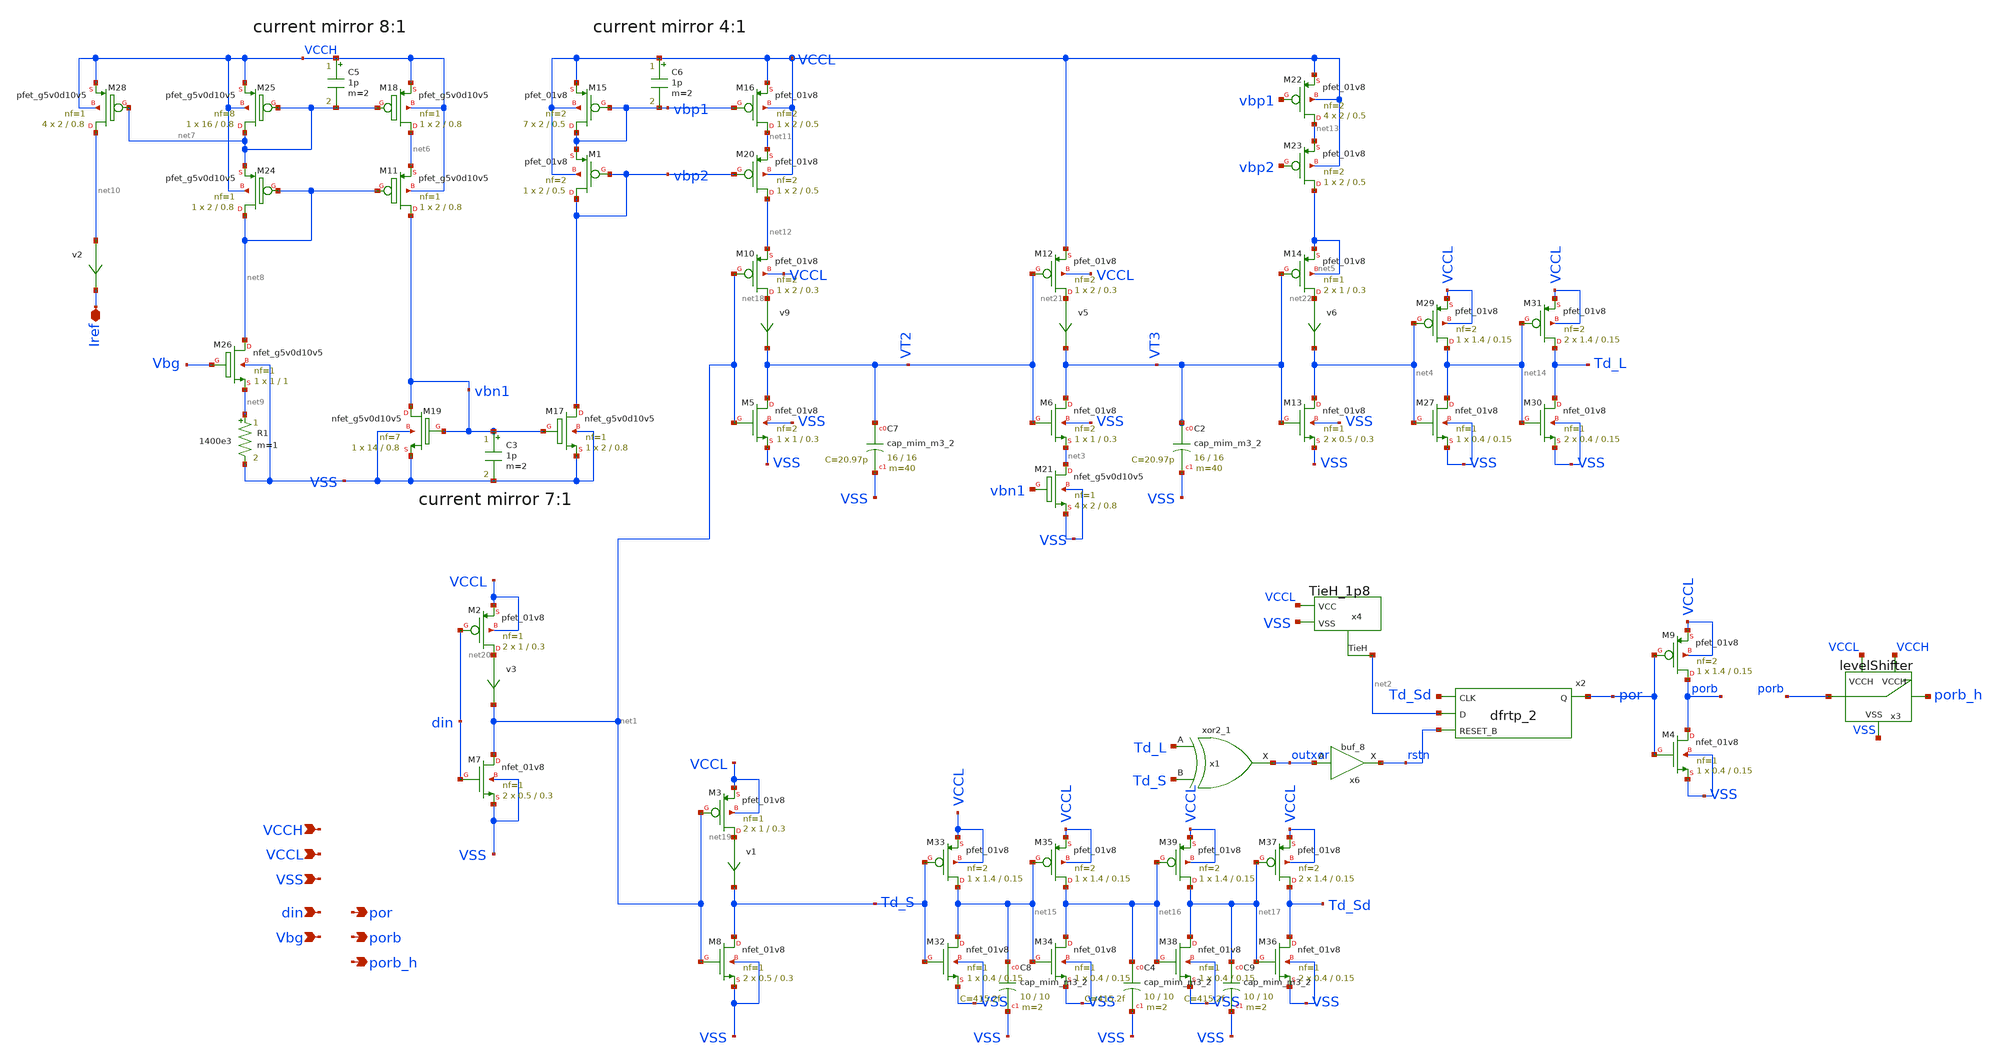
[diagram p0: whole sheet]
** sch_path: xschem/delayPulse.sch
**.subckt delayPulse VCCL VSS din Vbg por VCCH porb porb_h Iref
*.ipin VCCL
*.ipin VSS
*.ipin din
*.ipin Vbg
*.opin por
*.ipin VCCH
*.opin porb
*.opin porb_h
*.iopin Iref
v9 net18 VT2 0
.save i(v9)
v1 net19 Td_S 0
.save i(v1)
x2 Td_Sd net2 rstn VSS VSS VCCL VCCL por sky130_fd_sc_hd__dfrtp_2
v3 net20 net1 0
.save i(v3)
x1 Td_L Td_S VSS VSS VCCL VCCL outxor sky130_fd_sc_hd__xor2_1
x3 porb porb_h VCCL VSS VCCH levelShifter
XM2 net20 din VCCL VCCL sky130_fd_pr__pfet_01v8 L=0.3 W=1 nf=1 ad='int((nf+1)/2) * W/nf * 0.29' as='int((nf+2)/2) * W/nf * 0.29'
+ pd='2*int((nf+1)/2) * (W/nf + 0.29)' ps='2*int((nf+2)/2) * (W/nf + 0.29)' nrd='0.29 / W' nrs='0.29 / W'
+ sa=0 sb=0 sd=0 mult=2 m=2
XM3 net19 net1 VCCL VCCL sky130_fd_pr__pfet_01v8 L=0.3 W=1 nf=1 ad='int((nf+1)/2) * W/nf * 0.29' as='int((nf+2)/2) * W/nf * 0.29'
+ pd='2*int((nf+1)/2) * (W/nf + 0.29)' ps='2*int((nf+2)/2) * (W/nf + 0.29)' nrd='0.29 / W' nrs='0.29 / W'
+ sa=0 sb=0 sd=0 mult=2 m=2
XM5 VT2 net1 VSS VSS sky130_fd_pr__nfet_01v8 L=0.3 W=1 nf=2 ad='int((nf+1)/2) * W/nf * 0.29' as='int((nf+2)/2) * W/nf * 0.29'
+ pd='2*int((nf+1)/2) * (W/nf + 0.29)' ps='2*int((nf+2)/2) * (W/nf + 0.29)' nrd='0.29 / W' nrs='0.29 / W'
+ sa=0 sb=0 sd=0 mult=1 m=1
XM7 net1 din VSS VSS sky130_fd_pr__nfet_01v8 L=0.3 W=0.5 nf=1 ad='int((nf+1)/2) * W/nf * 0.29' as='int((nf+2)/2) * W/nf * 0.29'
+ pd='2*int((nf+1)/2) * (W/nf + 0.29)' ps='2*int((nf+2)/2) * (W/nf + 0.29)' nrd='0.29 / W' nrs='0.29 / W'
+ sa=0 sb=0 sd=0 mult=2 m=2
XM8 Td_S net1 VSS VSS sky130_fd_pr__nfet_01v8 L=0.3 W=0.5 nf=1 ad='int((nf+1)/2) * W/nf * 0.29' as='int((nf+2)/2) * W/nf * 0.29'
+ pd='2*int((nf+1)/2) * (W/nf + 0.29)' ps='2*int((nf+2)/2) * (W/nf + 0.29)' nrd='0.29 / W' nrs='0.29 / W'
+ sa=0 sb=0 sd=0 mult=2 m=2
XM10 net18 net1 net12 VCCL sky130_fd_pr__pfet_01v8 L=0.3 W=2 nf=2 ad='int((nf+1)/2) * W/nf * 0.29' as='int((nf+2)/2) * W/nf * 0.29'
+ pd='2*int((nf+1)/2) * (W/nf + 0.29)' ps='2*int((nf+2)/2) * (W/nf + 0.29)' nrd='0.29 / W' nrs='0.29 / W'
+ sa=0 sb=0 sd=0 mult=1 m=1
v5 net21 VT3 0
.save i(v5)
v6 net22 net4 0
.save i(v6)
XM13 net4 VT3 VSS VSS sky130_fd_pr__nfet_01v8 L=0.3 W=0.5 nf=1 ad='int((nf+1)/2) * W/nf * 0.29' as='int((nf+2)/2) * W/nf * 0.29'
+ pd='2*int((nf+1)/2) * (W/nf + 0.29)' ps='2*int((nf+2)/2) * (W/nf + 0.29)' nrd='0.29 / W' nrs='0.29 / W'
+ sa=0 sb=0 sd=0 mult=2 m=2
XM14 net22 VT3 net5 net5 sky130_fd_pr__pfet_01v8 L=0.3 W=1 nf=1 ad='int((nf+1)/2) * W/nf * 0.29' as='int((nf+2)/2) * W/nf * 0.29'
+ pd='2*int((nf+1)/2) * (W/nf + 0.29)' ps='2*int((nf+2)/2) * (W/nf + 0.29)' nrd='0.29 / W' nrs='0.29 / W'
+ sa=0 sb=0 sd=0 mult=2 m=2
x4 net2 VSS VCCL TieH_1p8
XM4 porb por VSS VSS sky130_fd_pr__nfet_01v8 L=0.15 W=0.4 nf=1 ad='int((nf+1)/2) * W/nf * 0.29' as='int((nf+2)/2) * W/nf * 0.29'
+ pd='2*int((nf+1)/2) * (W/nf + 0.29)' ps='2*int((nf+2)/2) * (W/nf + 0.29)' nrd='0.29 / W' nrs='0.29 / W'
+ sa=0 sb=0 sd=0 mult=1 m=1
XM9 porb por VCCL VCCL sky130_fd_pr__pfet_01v8 L=0.15 W=1.4 nf=2 ad='int((nf+1)/2) * W/nf * 0.29' as='int((nf+2)/2) * W/nf * 0.29'
+ pd='2*int((nf+1)/2) * (W/nf + 0.29)' ps='2*int((nf+2)/2) * (W/nf + 0.29)' nrd='0.29 / W' nrs='0.29 / W'
+ sa=0 sb=0 sd=0 mult=1 m=1
v2 net10 Iref 0
.save i(v2)
XM11 vbn1 net8 net6 VCCH sky130_fd_pr__pfet_g5v0d10v5 L=0.8 W=2 nf=1 ad='int((nf+1)/2) * W/nf * 0.29'
+ as='int((nf+2)/2) * W/nf * 0.29' pd='2*int((nf+1)/2) * (W/nf + 0.29)' ps='2*int((nf+2)/2) * (W/nf + 0.29)'
+ nrd='0.29 / W' nrs='0.29 / W' sa=0 sb=0 sd=0 mult=1 m=1
XM17 vbp2 vbn1 VSS VSS sky130_fd_pr__nfet_g5v0d10v5 L=0.8 W=2 nf=1 ad='int((nf+1)/2) * W/nf * 0.29' as='int((nf+2)/2) * W/nf * 0.29'
+ pd='2*int((nf+1)/2) * (W/nf + 0.29)' ps='2*int((nf+2)/2) * (W/nf + 0.29)' nrd='0.29 / W' nrs='0.29 / W'
+ sa=0 sb=0 sd=0 mult=1 m=1
XM18 net6 net7 VCCH VCCH sky130_fd_pr__pfet_g5v0d10v5 L=0.8 W=2 nf=1 ad='int((nf+1)/2) * W/nf * 0.29'
+ as='int((nf+2)/2) * W/nf * 0.29' pd='2*int((nf+1)/2) * (W/nf + 0.29)' ps='2*int((nf+2)/2) * (W/nf + 0.29)'
+ nrd='0.29 / W' nrs='0.29 / W' sa=0 sb=0 sd=0 mult=1 m=1
XM19 vbn1 vbn1 VSS VSS sky130_fd_pr__nfet_g5v0d10v5 L=0.8 W=14 nf=7 ad='int((nf+1)/2) * W/nf * 0.29'
+ as='int((nf+2)/2) * W/nf * 0.29' pd='2*int((nf+1)/2) * (W/nf + 0.29)' ps='2*int((nf+2)/2) * (W/nf + 0.29)'
+ nrd='0.29 / W' nrs='0.29 / W' sa=0 sb=0 sd=0 mult=1 m=1
XM24 net8 net8 net7 VCCH sky130_fd_pr__pfet_g5v0d10v5 L=0.8 W=2 nf=1 ad='int((nf+1)/2) * W/nf * 0.29'
+ as='int((nf+2)/2) * W/nf * 0.29' pd='2*int((nf+1)/2) * (W/nf + 0.29)' ps='2*int((nf+2)/2) * (W/nf + 0.29)'
+ nrd='0.29 / W' nrs='0.29 / W' sa=0 sb=0 sd=0 mult=1 m=1
XM25 net7 net7 VCCH VCCH sky130_fd_pr__pfet_g5v0d10v5 L=0.8 W=16 nf=8 ad='int((nf+1)/2) * W/nf * 0.29'
+ as='int((nf+2)/2) * W/nf * 0.29' pd='2*int((nf+1)/2) * (W/nf + 0.29)' ps='2*int((nf+2)/2) * (W/nf + 0.29)'
+ nrd='0.29 / W' nrs='0.29 / W' sa=0 sb=0 sd=0 mult=1 m=1
XM26 net8 Vbg net9 VSS sky130_fd_pr__nfet_g5v0d10v5 L=1 W=1 nf=1 ad='int((nf+1)/2) * W/nf * 0.29' as='int((nf+2)/2) * W/nf * 0.29'
+ pd='2*int((nf+1)/2) * (W/nf + 0.29)' ps='2*int((nf+2)/2) * (W/nf + 0.29)' nrd='0.29 / W' nrs='0.29 / W'
+ sa=0 sb=0 sd=0 mult=1 m=1
R1 net9 VSS 1400e3 m=1
XM28 net10 net7 VCCH VCCH sky130_fd_pr__pfet_g5v0d10v5 L=0.8 W=2 nf=1 ad='int((nf+1)/2) * W/nf * 0.29'
+ as='int((nf+2)/2) * W/nf * 0.29' pd='2*int((nf+1)/2) * (W/nf + 0.29)' ps='2*int((nf+2)/2) * (W/nf + 0.29)'
+ nrd='0.29 / W' nrs='0.29 / W' sa=0 sb=0 sd=0 mult=4 m=4
XM6 VT3 VT2 net3 VSS sky130_fd_pr__nfet_01v8 L=0.3 W=1 nf=2 ad='int((nf+1)/2) * W/nf * 0.29' as='int((nf+2)/2) * W/nf * 0.29'
+ pd='2*int((nf+1)/2) * (W/nf + 0.29)' ps='2*int((nf+2)/2) * (W/nf + 0.29)' nrd='0.29 / W' nrs='0.29 / W'
+ sa=0 sb=0 sd=0 mult=1 m=1
XM12 net21 VT2 VCCL VCCL sky130_fd_pr__pfet_01v8 L=0.3 W=2 nf=2 ad='int((nf+1)/2) * W/nf * 0.29' as='int((nf+2)/2) * W/nf * 0.29'
+ pd='2*int((nf+1)/2) * (W/nf + 0.29)' ps='2*int((nf+2)/2) * (W/nf + 0.29)' nrd='0.29 / W' nrs='0.29 / W'
+ sa=0 sb=0 sd=0 mult=1 m=1
XM1 vbp2 vbp2 vbp1 VCCL sky130_fd_pr__pfet_01v8 L=0.5 W=2 nf=2 ad='int((nf+1)/2) * W/nf * 0.29' as='int((nf+2)/2) * W/nf * 0.29'
+ pd='2*int((nf+1)/2) * (W/nf + 0.29)' ps='2*int((nf+2)/2) * (W/nf + 0.29)' nrd='0.29 / W' nrs='0.29 / W'
+ sa=0 sb=0 sd=0 mult=1 m=1
XM15 vbp1 vbp1 VCCL VCCL sky130_fd_pr__pfet_01v8 L=0.5 W=2 nf=2 ad='int((nf+1)/2) * W/nf * 0.29' as='int((nf+2)/2) * W/nf * 0.29'
+ pd='2*int((nf+1)/2) * (W/nf + 0.29)' ps='2*int((nf+2)/2) * (W/nf + 0.29)' nrd='0.29 / W' nrs='0.29 / W'
+ sa=0 sb=0 sd=0 mult=7 m=7
XM16 net11 vbp1 VCCL VCCL sky130_fd_pr__pfet_01v8 L=0.5 W=2 nf=2 ad='int((nf+1)/2) * W/nf * 0.29' as='int((nf+2)/2) * W/nf * 0.29'
+ pd='2*int((nf+1)/2) * (W/nf + 0.29)' ps='2*int((nf+2)/2) * (W/nf + 0.29)' nrd='0.29 / W' nrs='0.29 / W'
+ sa=0 sb=0 sd=0 mult=1 m=1
XM20 net12 vbp2 net11 VCCL sky130_fd_pr__pfet_01v8 L=0.5 W=2 nf=2 ad='int((nf+1)/2) * W/nf * 0.29' as='int((nf+2)/2) * W/nf * 0.29'
+ pd='2*int((nf+1)/2) * (W/nf + 0.29)' ps='2*int((nf+2)/2) * (W/nf + 0.29)' nrd='0.29 / W' nrs='0.29 / W'
+ sa=0 sb=0 sd=0 mult=1 m=1
XM21 net3 vbn1 VSS VSS sky130_fd_pr__nfet_g5v0d10v5 L=0.8 W=2 nf=1 ad='int((nf+1)/2) * W/nf * 0.29' as='int((nf+2)/2) * W/nf * 0.29'
+ pd='2*int((nf+1)/2) * (W/nf + 0.29)' ps='2*int((nf+2)/2) * (W/nf + 0.29)' nrd='0.29 / W' nrs='0.29 / W'
+ sa=0 sb=0 sd=0 mult=4 m=4
C3 vbn1 VSS 1p m=2
C5 VCCH net7 1p m=2
C6 VCCL vbp1 1p m=2
XM22 net13 vbp1 VCCL VCCL sky130_fd_pr__pfet_01v8 L=0.5 W=2 nf=2 ad='int((nf+1)/2) * W/nf * 0.29' as='int((nf+2)/2) * W/nf * 0.29'
+ pd='2*int((nf+1)/2) * (W/nf + 0.29)' ps='2*int((nf+2)/2) * (W/nf + 0.29)' nrd='0.29 / W' nrs='0.29 / W'
+ sa=0 sb=0 sd=0 mult=4 m=4
XM23 net5 vbp2 net13 VCCL sky130_fd_pr__pfet_01v8 L=0.5 W=2 nf=2 ad='int((nf+1)/2) * W/nf * 0.29' as='int((nf+2)/2) * W/nf * 0.29'
+ pd='2*int((nf+1)/2) * (W/nf + 0.29)' ps='2*int((nf+2)/2) * (W/nf + 0.29)' nrd='0.29 / W' nrs='0.29 / W'
+ sa=0 sb=0 sd=0 mult=1 m=1
XM27 net14 net4 VSS VSS sky130_fd_pr__nfet_01v8 L=0.15 W=0.4 nf=1 ad='int((nf+1)/2) * W/nf * 0.29' as='int((nf+2)/2) * W/nf * 0.29'
+ pd='2*int((nf+1)/2) * (W/nf + 0.29)' ps='2*int((nf+2)/2) * (W/nf + 0.29)' nrd='0.29 / W' nrs='0.29 / W'
+ sa=0 sb=0 sd=0 mult=1 m=1
XM29 net14 net4 VCCL VCCL sky130_fd_pr__pfet_01v8 L=0.15 W=1.4 nf=2 ad='int((nf+1)/2) * W/nf * 0.29'
+ as='int((nf+2)/2) * W/nf * 0.29' pd='2*int((nf+1)/2) * (W/nf + 0.29)' ps='2*int((nf+2)/2) * (W/nf + 0.29)'
+ nrd='0.29 / W' nrs='0.29 / W' sa=0 sb=0 sd=0 mult=1 m=1
XM30 Td_L net14 VSS VSS sky130_fd_pr__nfet_01v8 L=0.15 W=0.4 nf=1 ad='int((nf+1)/2) * W/nf * 0.29' as='int((nf+2)/2) * W/nf * 0.29'
+ pd='2*int((nf+1)/2) * (W/nf + 0.29)' ps='2*int((nf+2)/2) * (W/nf + 0.29)' nrd='0.29 / W' nrs='0.29 / W'
+ sa=0 sb=0 sd=0 mult=2 m=2
XM31 Td_L net14 VCCL VCCL sky130_fd_pr__pfet_01v8 L=0.15 W=1.4 nf=2 ad='int((nf+1)/2) * W/nf * 0.29'
+ as='int((nf+2)/2) * W/nf * 0.29' pd='2*int((nf+1)/2) * (W/nf + 0.29)' ps='2*int((nf+2)/2) * (W/nf + 0.29)'
+ nrd='0.29 / W' nrs='0.29 / W' sa=0 sb=0 sd=0 mult=2 m=2
XM32 net15 Td_S VSS VSS sky130_fd_pr__nfet_01v8 L=0.15 W=0.4 nf=1 ad='int((nf+1)/2) * W/nf * 0.29' as='int((nf+2)/2) * W/nf * 0.29'
+ pd='2*int((nf+1)/2) * (W/nf + 0.29)' ps='2*int((nf+2)/2) * (W/nf + 0.29)' nrd='0.29 / W' nrs='0.29 / W'
+ sa=0 sb=0 sd=0 mult=1 m=1
XM33 net15 Td_S VCCL VCCL sky130_fd_pr__pfet_01v8 L=0.15 W=1.4 nf=2 ad='int((nf+1)/2) * W/nf * 0.29'
+ as='int((nf+2)/2) * W/nf * 0.29' pd='2*int((nf+1)/2) * (W/nf + 0.29)' ps='2*int((nf+2)/2) * (W/nf + 0.29)'
+ nrd='0.29 / W' nrs='0.29 / W' sa=0 sb=0 sd=0 mult=1 m=1
XM34 net16 net15 VSS VSS sky130_fd_pr__nfet_01v8 L=0.15 W=0.4 nf=1 ad='int((nf+1)/2) * W/nf * 0.29' as='int((nf+2)/2) * W/nf * 0.29'
+ pd='2*int((nf+1)/2) * (W/nf + 0.29)' ps='2*int((nf+2)/2) * (W/nf + 0.29)' nrd='0.29 / W' nrs='0.29 / W'
+ sa=0 sb=0 sd=0 mult=1 m=1
XM35 net16 net15 VCCL VCCL sky130_fd_pr__pfet_01v8 L=0.15 W=1.4 nf=2 ad='int((nf+1)/2) * W/nf * 0.29'
+ as='int((nf+2)/2) * W/nf * 0.29' pd='2*int((nf+1)/2) * (W/nf + 0.29)' ps='2*int((nf+2)/2) * (W/nf + 0.29)'
+ nrd='0.29 / W' nrs='0.29 / W' sa=0 sb=0 sd=0 mult=1 m=1
XM36 Td_Sd net17 VSS VSS sky130_fd_pr__nfet_01v8 L=0.15 W=0.4 nf=1 ad='int((nf+1)/2) * W/nf * 0.29' as='int((nf+2)/2) * W/nf * 0.29'
+ pd='2*int((nf+1)/2) * (W/nf + 0.29)' ps='2*int((nf+2)/2) * (W/nf + 0.29)' nrd='0.29 / W' nrs='0.29 / W'
+ sa=0 sb=0 sd=0 mult=2 m=2
XM37 Td_Sd net17 VCCL VCCL sky130_fd_pr__pfet_01v8 L=0.15 W=1.4 nf=2 ad='int((nf+1)/2) * W/nf * 0.29'
+ as='int((nf+2)/2) * W/nf * 0.29' pd='2*int((nf+1)/2) * (W/nf + 0.29)' ps='2*int((nf+2)/2) * (W/nf + 0.29)'
+ nrd='0.29 / W' nrs='0.29 / W' sa=0 sb=0 sd=0 mult=2 m=2
XM38 net17 net16 VSS VSS sky130_fd_pr__nfet_01v8 L=0.15 W=0.4 nf=1 ad='int((nf+1)/2) * W/nf * 0.29' as='int((nf+2)/2) * W/nf * 0.29'
+ pd='2*int((nf+1)/2) * (W/nf + 0.29)' ps='2*int((nf+2)/2) * (W/nf + 0.29)' nrd='0.29 / W' nrs='0.29 / W'
+ sa=0 sb=0 sd=0 mult=1 m=1
XM39 net17 net16 VCCL VCCL sky130_fd_pr__pfet_01v8 L=0.15 W=1.4 nf=2 ad='int((nf+1)/2) * W/nf * 0.29'
+ as='int((nf+2)/2) * W/nf * 0.29' pd='2*int((nf+1)/2) * (W/nf + 0.29)' ps='2*int((nf+2)/2) * (W/nf + 0.29)'
+ nrd='0.29 / W' nrs='0.29 / W' sa=0 sb=0 sd=0 mult=1 m=1
x6 outxor VSS VSS VCCL VCCL rstn sky130_fd_sc_hvl__buf_8
XC4 net16 VSS sky130_fd_pr__cap_mim_m3_2 W=10 L=10 MF=2 m=2
XC7 VT2 VSS sky130_fd_pr__cap_mim_m3_2 W=16 L=16 MF=40 m=40
XC2 VT3 VSS sky130_fd_pr__cap_mim_m3_2 W=16 L=16 MF=40 m=40
XC8 net15 VSS sky130_fd_pr__cap_mim_m3_2 W=10 L=10 MF=2 m=2
XC9 net17 VSS sky130_fd_pr__cap_mim_m3_2 W=10 L=10 MF=2 m=2
**.ends
.end
